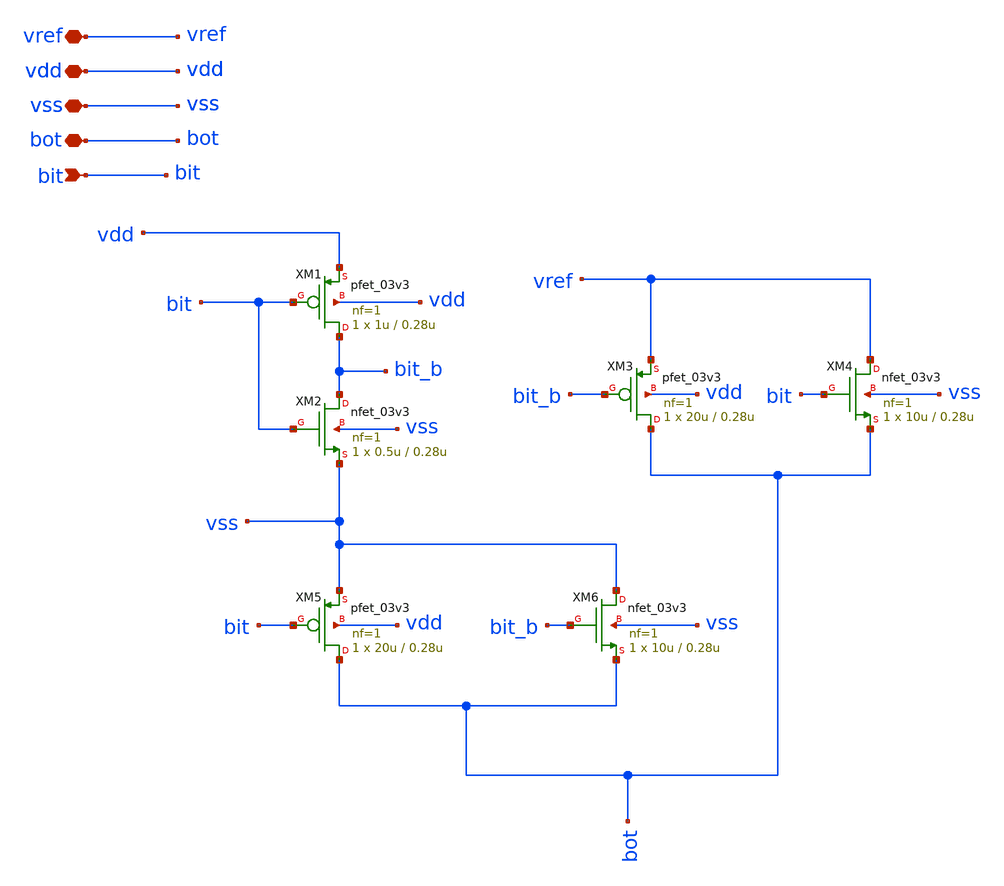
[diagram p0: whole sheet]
** sch_path: xschem/sar_adc/blocks/cdac/cdac_switch_1b.sch
**.subckt cdac_switch_1b vdd vss vref bit bot vdd vss
*.iopin vdd
*.iopin vss
*.iopin vref
*.ipin bit
*.iopin bot
*.iopin vdd
*.iopin vss
XM1 bit_b bit vdd vdd pfet_03v3 L=0.28u W=1u nf=1 ad='int((nf+1)/2) * W/nf * 0.18u' as='int((nf+2)/2) * W/nf * 0.18u'
+ pd='2*int((nf+1)/2) * (W/nf + 0.18u)' ps='2*int((nf+2)/2) * (W/nf + 0.18u)' nrd='0.18u / W' nrs='0.18u / W'
+ sa=0 sb=0 sd=0 m=1
XM2 bit_b bit vss vss nfet_03v3 L=0.28u W=0.5u nf=1 ad='int((nf+1)/2) * W/nf * 0.18u' as='int((nf+2)/2) * W/nf * 0.18u'
+ pd='2*int((nf+1)/2) * (W/nf + 0.18u)' ps='2*int((nf+2)/2) * (W/nf + 0.18u)' nrd='0.18u / W' nrs='0.18u / W'
+ sa=0 sb=0 sd=0 m=1
XM3 bot bit_b vref vdd pfet_03v3 L=0.28u W=20u nf=1 ad='int((nf+1)/2) * W/nf * 0.18u' as='int((nf+2)/2) * W/nf * 0.18u'
+ pd='2*int((nf+1)/2) * (W/nf + 0.18u)' ps='2*int((nf+2)/2) * (W/nf + 0.18u)' nrd='0.18u / W' nrs='0.18u / W'
+ sa=0 sb=0 sd=0 m=1
XM4 vref bit bot vss nfet_03v3 L=0.28u W=10u nf=1 ad='int((nf+1)/2) * W/nf * 0.18u' as='int((nf+2)/2) * W/nf * 0.18u'
+ pd='2*int((nf+1)/2) * (W/nf + 0.18u)' ps='2*int((nf+2)/2) * (W/nf + 0.18u)' nrd='0.18u / W' nrs='0.18u / W'
+ sa=0 sb=0 sd=0 m=1
XM5 bot bit vss vdd pfet_03v3 L=0.28u W=20u nf=1 ad='int((nf+1)/2) * W/nf * 0.18u' as='int((nf+2)/2) * W/nf * 0.18u'
+ pd='2*int((nf+1)/2) * (W/nf + 0.18u)' ps='2*int((nf+2)/2) * (W/nf + 0.18u)' nrd='0.18u / W' nrs='0.18u / W'
+ sa=0 sb=0 sd=0 m=1
XM6 vss bit_b bot vss nfet_03v3 L=0.28u W=10u nf=1 ad='int((nf+1)/2) * W/nf * 0.18u' as='int((nf+2)/2) * W/nf * 0.18u'
+ pd='2*int((nf+1)/2) * (W/nf + 0.18u)' ps='2*int((nf+2)/2) * (W/nf + 0.18u)' nrd='0.18u / W' nrs='0.18u / W'
+ sa=0 sb=0 sd=0 m=1
**.ends
.end
